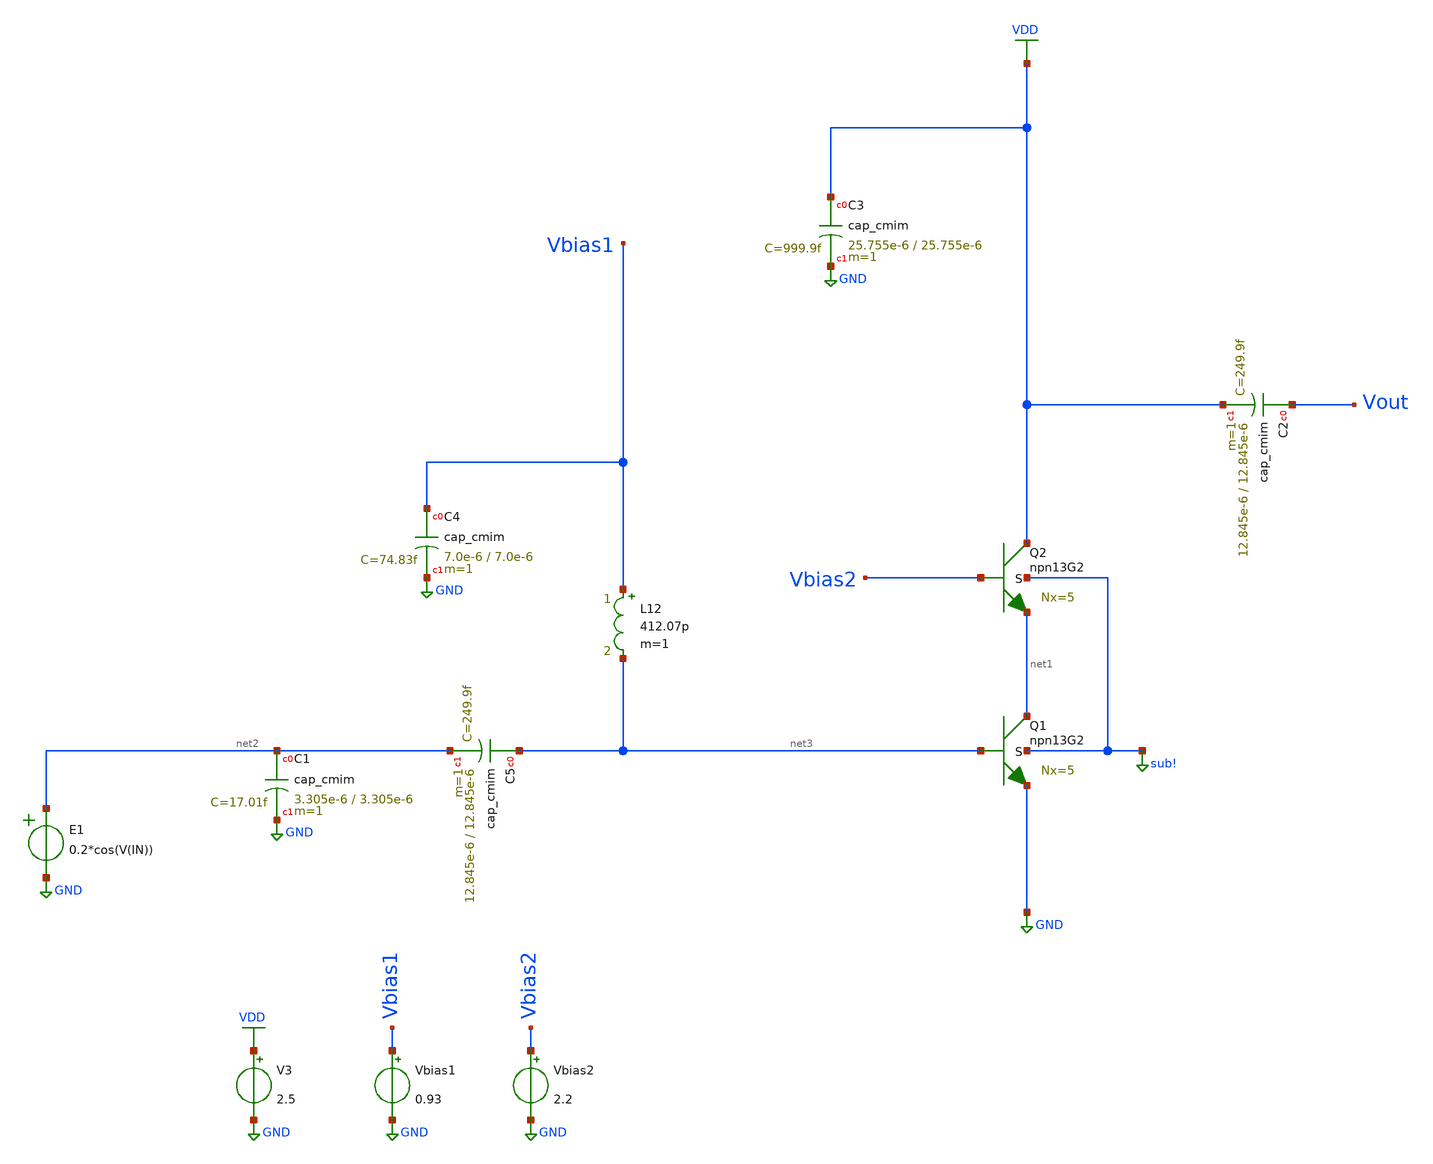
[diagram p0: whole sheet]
** sch_path: LNA_120GHz/design_data/xschem/LNA_manael.sch
**.subckt LNA_manael
XQ1 net1 net3 GND sub! npn13G2 Nx=5 mm_ok=1
XQ2 VDD Vbias2 net1 sub! npn13G2 Nx=5 mm_ok=1
XC1 net2 GND cap_cmim w=3.305e-6 l=3.305e-6 m=1 mm_ok=1
XC2 Vout VDD cap_cmim w=12.845e-6 l=12.845e-6 m=1 mm_ok=1
XC3 VDD GND cap_cmim w=25.755e-6 l=25.755e-6 m=1 mm_ok=1
XC4 Vbias1 GND cap_cmim w=7.0e-6 l=7.0e-6 m=1 mm_ok=1
Vbias1 Vbias1 GND 0.93
Vbias2 Vbias2 GND 2.2
V3 VDD GND 2.5
E1 net2 GND VOL=' 0.2*cos(V(IN)) '
XC5 net3 net2 cap_cmim w=12.845e-6 l=12.845e-6 m=1 mm_ok=1
L12 Vbias1 net3 412.07p m=1
**.ends
.GLOBAL GND
.GLOBAL VDD
.GLOBAL sub!
.end
